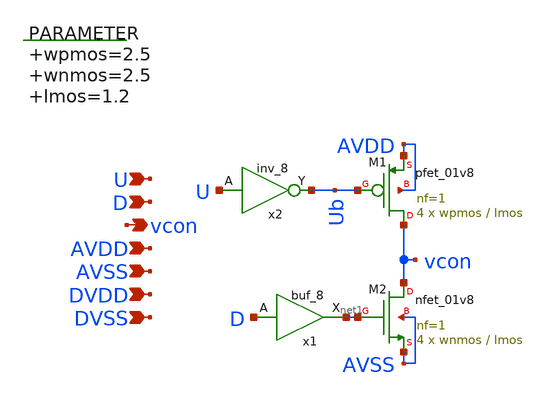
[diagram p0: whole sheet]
** sch_path: xschem/charge_pump.sch
**.subckt charge_pump U D vcon AVDD AVSS DVDD DVSS
*.ipin U
*.ipin D
*.opin vcon
*.ipin AVDD
*.ipin AVSS
*.ipin DVDD
*.ipin DVSS
XM1 vcon Ub AVDD AVDD sky130_fd_pr__pfet_01v8 L=lmos W=wpmos nf=1 ad='int((nf+1)/2) * W/nf * 0.29' as='int((nf+2)/2) * W/nf * 0.29'
+ pd='2*int((nf+1)/2) * (W/nf + 0.29)' ps='2*int((nf+2)/2) * (W/nf + 0.29)' nrd='0.29 / W' nrs='0.29 / W'
+ sa=0 sb=0 sd=0 mult=4 m=4
XM2 vcon net1 AVSS AVSS sky130_fd_pr__nfet_01v8 L=lmos W=wnmos nf=1 ad='int((nf+1)/2) * W/nf * 0.29'
+ as='int((nf+2)/2) * W/nf * 0.29' pd='2*int((nf+1)/2) * (W/nf + 0.29)' ps='2*int((nf+2)/2) * (W/nf + 0.29)'
+ nrd='0.29 / W' nrs='0.29 / W' sa=0 sb=0 sd=0 mult=4 m=4
.param wpmos=2.5 wnmos=2.5 lmos=1.2
x1 D DVSS DVSS DVDD DVDD net1 sky130_fd_sc_hd__buf_8
x2 U DVSS DVSS DVDD DVDD Ub sky130_fd_sc_hd__inv_8
**.ends
.end
